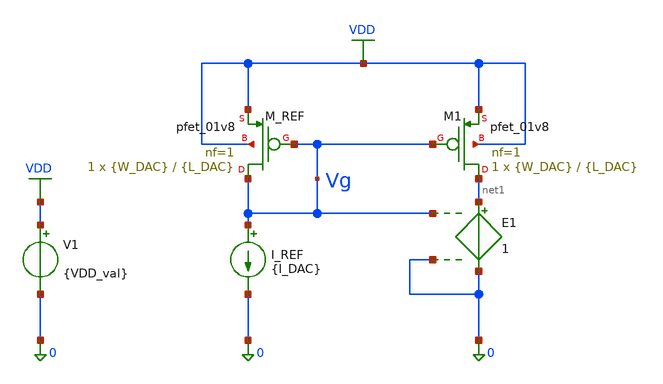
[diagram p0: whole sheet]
** sch_path: designs_backup/designs/lab2/lab2_mismatch.sch
**.subckt lab2_mismatch
I_REF Vg 0 {I_DAC}
E1 net1 0 Vg 0 1
V1 VDD 0 {VDD_val}
XM1 net1 Vg VDD VDD sky130_fd_pr__pfet_01v8 L={L_DAC} W={W_DAC} nf=1 ad='int((1 + 1)/2) * {W_DAC} / 1 * 0.29'
+ as='int((1 + 2)/2) * {W_DAC} / 1 * 0.29' pd='2*int((1 + 1)/2) * ({W_DAC} / 1 + 0.29)' ps='2*int((1 + 2)/2) * ({W_DAC} / 1 + 0.29)'
+ nrd='0.29 / {W_DAC} ' nrs='0.29 / {W_DAC} ' sa=0 sb=0 sd=0 mult=1 m=1
XM_REF Vg Vg VDD VDD sky130_fd_pr__pfet_01v8 L={L_DAC} W={W_DAC} nf=1 ad='int((1 + 1)/2) * {W_DAC} / 1 * 0.29'
+ as='int((1 + 2)/2) * {W_DAC} / 1 * 0.29' pd='2*int((1 + 1)/2) * ({W_DAC} / 1 + 0.29)' ps='2*int((1 + 2)/2) * ({W_DAC} / 1 + 0.29)'
+ nrd='0.29 / {W_DAC} ' nrs='0.29 / {W_DAC} ' sa=0 sb=0 sd=0 mult=1 m=1
**** begin user architecture code

** opencircuitdesign pdks install
.lib $::SKYWATER_MODELS/sky130.lib.spice tt_mm

* force Mismatch/Process/Mismatch+Process config
.param mc_mm_switch = 1
.param mc_pr_switch = 0



.param W_DAC = 0.42 L_DAC = 0.18
.param I_DAC = 100n
.param VDD_val = 1.8
.options savecurrents

.control
  let runs = 100
  shell mkdir -p /foss/designs/lab2/results/1.8
  shell rm -f /foss/designs/lab2/results/1.8/M1_stats.dat
+ /foss/designs/lab2/results/1.8/M1_Iruns.dat

  foreach idac_val 100n 10u
    foreach case_idx 1 2 3
      if $case_idx = 1
        alterparam W_DAC = 0.42
        alterparam L_DAC = 0.18
      end
      if $case_idx = 2
        alterparam W_DAC = 5.0
        alterparam L_DAC = 2.0
      end
      if $case_idx = 3
        alterparam W_DAC = 2.0
        alterparam L_DAC = 5.0
      end
      alterparam I_DAC = $idac_val
      * allocate vector for currents
      let Ivec = vector(runs)
      let r = 0

      * reset and op to apply W/L changes
      reset
      op
      let scale = 1e6
      let W = @m.xm1.msky130_fd_pr__pfet_01v8[w]*scale
      let L = @m.xm1.msky130_fd_pr__pfet_01v8[l]*scale
      echo ----- W/L= $&W / $&L IDAC= $idac_val ----- >> /foss/designs/lab2/results/1.8/M1_Iruns.dat
      echo ----- W/L= $&W / $&L IDAC= $idac_val ----- >> /foss/designs/lab2/results/1.8/M1_stats.dat
      dowhile r < runs
        reset
        op
        let Ivec[r] = @m.xm1.msky130_fd_pr__pfet_01v8[id]
        let curI = Ivec[r]
        set appendwrite
        echo RUN= $&r I= $&curI >> /foss/designs/lab2/results/1.8/M1_Iruns.dat
        let r = r + 1
      end

      * calculate stats
      let avgI = mean(Ivec)
      let sigI = stddev(Ivec)
      let ratio = sigI/avgI
      * vecmin() does the same as minimum() ; analogically is maximum() and vecmax()
      let minI = minimum(Ivec)
      let maxI = maximum(Ivec)

      echo MIN= $&minI MAX= $&maxI AVG= $&avgI SIGMA= $&sigI sigma/AVG= $&ratio >>
+ /foss/designs/lab2/results/1.8/M1_stats.dat
      echo >> /foss/designs/lab2/results/1.8/M1_stats.dat
    end
  end
.endc


**** end user architecture code
**.ends
.GLOBAL VDD
.end
